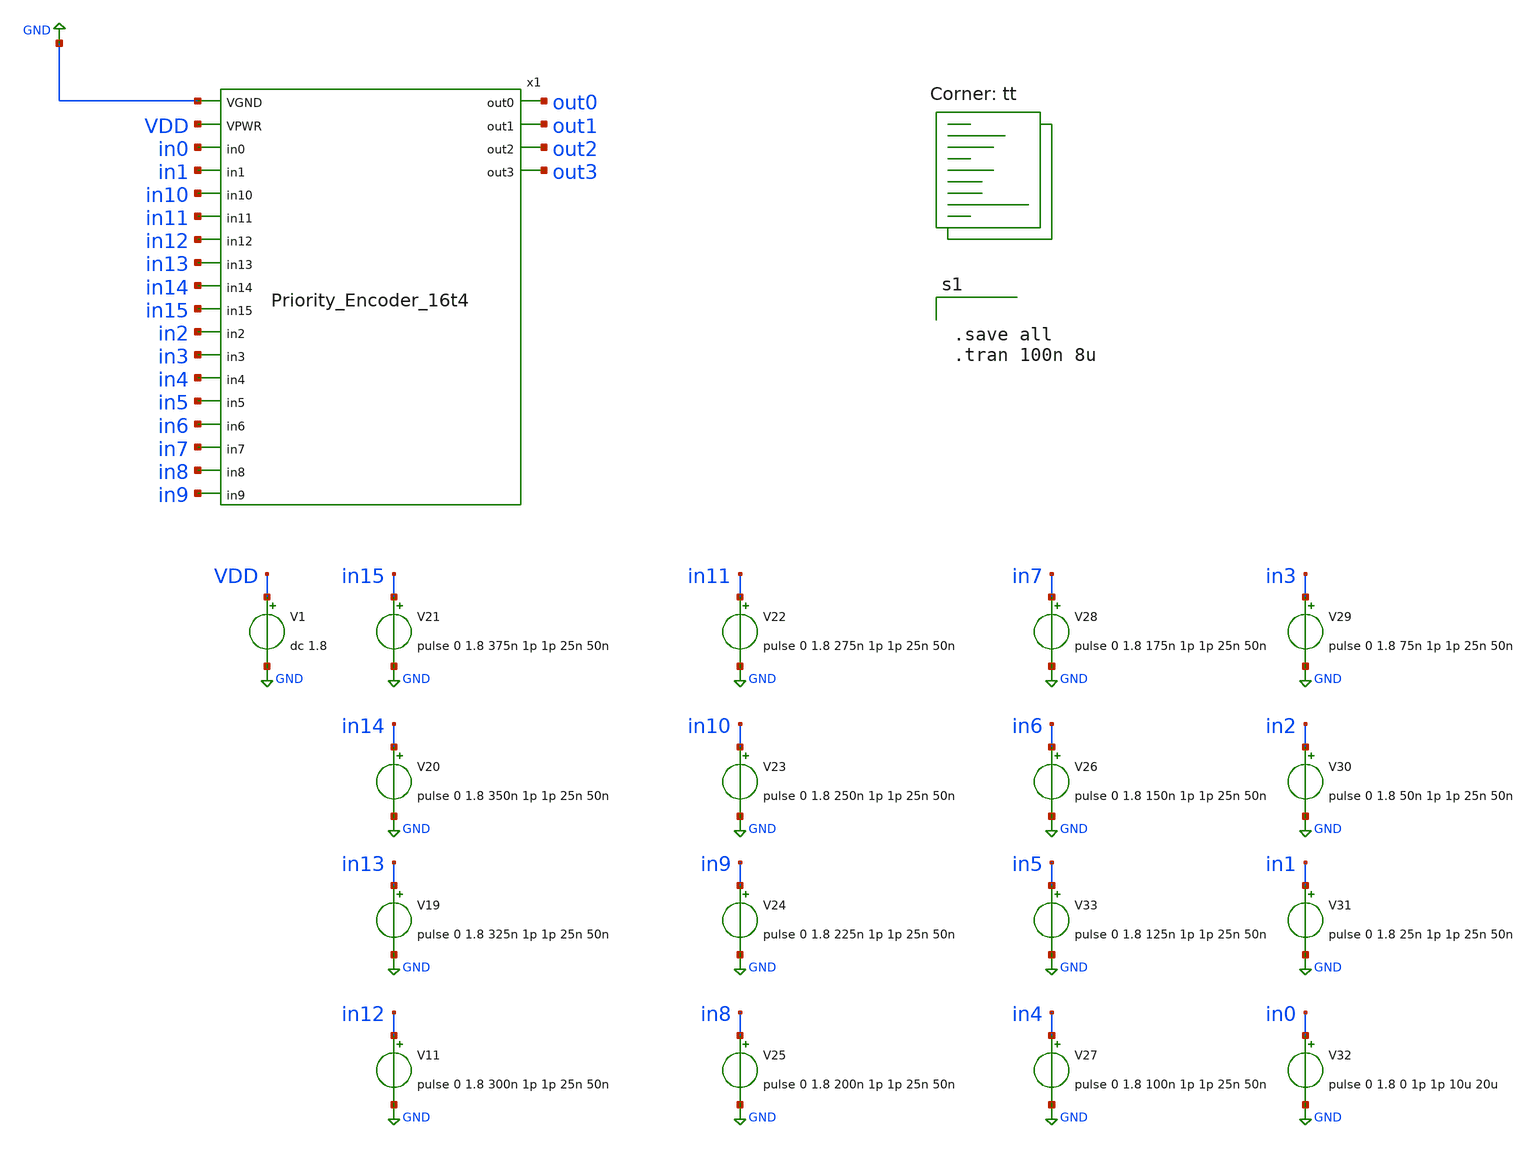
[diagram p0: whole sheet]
** sch_path: xschem/DataConverters/P_Encoder_Test.sch
**.subckt P_Encoder_Test
V1 VDD GND dc 1.8
x1 GND VDD in0 in1 in10 in11 in12 in13 in14 in15 in2 in3 in4 in5 in6 in7 in8 in9 out0 out1 out2 out3
+ Priority_Encoder_16t4
V11 in12 GND pulse 0 1.8 300n 1p 1p 25n 50n
V19 in13 GND pulse 0 1.8 325n 1p 1p 25n 50n
V20 in14 GND pulse 0 1.8 350n 1p 1p 25n 50n
V21 in15 GND pulse 0 1.8 375n 1p 1p 25n 50n
V22 in11 GND pulse 0 1.8 275n 1p 1p 25n 50n
V23 in10 GND pulse 0 1.8 250n 1p 1p 25n 50n
V24 in9 GND pulse 0 1.8 225n 1p 1p 25n 50n
V25 in8 GND pulse 0 1.8 200n 1p 1p 25n 50n
V26 in6 GND pulse 0 1.8 150n 1p 1p 25n 50n
V27 in4 GND pulse 0 1.8 100n 1p 1p 25n 50n
V28 in7 GND pulse 0 1.8 175n 1p 1p 25n 50n
V29 in3 GND pulse 0 1.8 75n 1p 1p 25n 50n
V30 in2 GND pulse 0 1.8 50n 1p 1p 25n 50n
V31 in1 GND pulse 0 1.8 25n 1p 1p 25n 50n
V32 in0 GND pulse 0 1.8 0 1p 1p 10u 20u
V33 in5 GND pulse 0 1.8 125n 1p 1p 25n 50n
**** begin user architecture code
.lib $::SKYWATER_MODELS/sky130.lib.spice tt


.save all
.tran 100n 8u



** opencircuitdesign pdks install
.include $::SKYWATER_STDCELLS/sky130_fd_sc_hd.spice


**** end user architecture code
**.ends

* expanding   symbol:  DataConverters/Priority_Encoder_16t4.sym # of pins=22
** sym_path: xschem/Priority_Encoder_16t4.sym
** sch_path: xschem/Priority_Encoder_16t4.sch
.subckt Priority_Encoder_16t4 VGND VPWR in0 in1 in10 in11 in12 in13 in14 in15 in2 in3 in4 in5 in6
+ in7 in8 in9 out0 out1 out2 out3
*.ipin VGND
*.ipin VPWR
*.ipin in0
*.ipin in1
*.ipin in10
*.ipin in11
*.ipin in12
*.ipin in13
*.ipin in14
*.ipin in15
*.ipin in2
*.ipin in3
*.ipin in4
*.ipin in5
*.ipin in6
*.ipin in7
*.ipin in8
*.ipin in9
*.opin out0
*.opin out1
*.opin out2
*.opin out3
X_16_ net8 VGND VGND VPWR VPWR _00_ sky130_fd_sc_hd__inv_2
X_17_ net4 net5 VGND VGND VPWR VPWR _01_ sky130_fd_sc_hd__nor2_1
X_18_ net4 net5 net6 net7 VGND VGND VPWR VPWR _02_ sky130_fd_sc_hd__or4_1
X_19_ net2 net3 VGND VGND VPWR VPWR _03_ sky130_fd_sc_hd__nor2_1
X_20_ net15 net14 VGND VGND VPWR VPWR _04_ sky130_fd_sc_hd__nor2_1
X_21_ net15 net14 _02_ _03_ VGND VGND VPWR VPWR net19 sky130_fd_sc_hd__or4b_2
X_22_ net11 net10 VGND VGND VPWR VPWR _05_ sky130_fd_sc_hd__nor2_1
X_23_ net13 net11 net10 net12 VGND VGND VPWR VPWR _06_ sky130_fd_sc_hd__or4_1
X_24_ _03_ _04_ _06_ _02_ VGND VGND VPWR VPWR net18 sky130_fd_sc_hd__a31o_1
X_25_ net9 net8 _05_ VGND VGND VPWR VPWR _07_ sky130_fd_sc_hd__o21a_1
X_26_ net13 net12 _07_ _04_ VGND VGND VPWR VPWR _08_ sky130_fd_sc_hd__o31a_1
X_27_ net2 net3 _08_ _01_ VGND VGND VPWR VPWR _09_ sky130_fd_sc_hd__o31a_1
X_28_ net6 net7 _09_ VGND VGND VPWR VPWR net17 sky130_fd_sc_hd__or3_1
X_29_ _00_ net1 net9 VGND VGND VPWR VPWR _10_ sky130_fd_sc_hd__a21oi_1
X_30_ net10 _10_ net11 VGND VGND VPWR VPWR _11_ sky130_fd_sc_hd__o21ba_1
X_31_ net12 _11_ net13 VGND VGND VPWR VPWR _12_ sky130_fd_sc_hd__o21ba_1
X_32_ net14 _12_ net15 VGND VGND VPWR VPWR _13_ sky130_fd_sc_hd__o21ba_1
X_33_ net2 _13_ net3 VGND VGND VPWR VPWR _14_ sky130_fd_sc_hd__o21ba_1
X_34_ net4 _14_ net5 VGND VGND VPWR VPWR _15_ sky130_fd_sc_hd__o21ba_1
X_35_ net6 _15_ net7 VGND VGND VPWR VPWR net16 sky130_fd_sc_hd__o21bai_2
Xinput1 in1 VGND VGND VPWR VPWR net1 sky130_fd_sc_hd__clkbuf_1
Xinput10 in4 VGND VGND VPWR VPWR net10 sky130_fd_sc_hd__buf_1
Xinput11 in5 VGND VGND VPWR VPWR net11 sky130_fd_sc_hd__buf_1
Xinput12 in6 VGND VGND VPWR VPWR net12 sky130_fd_sc_hd__buf_1
Xinput13 in7 VGND VGND VPWR VPWR net13 sky130_fd_sc_hd__clkbuf_1
Xinput14 in8 VGND VGND VPWR VPWR net14 sky130_fd_sc_hd__buf_1
Xinput15 in9 VGND VGND VPWR VPWR net15 sky130_fd_sc_hd__buf_1
Xinput2 in10 VGND VGND VPWR VPWR net2 sky130_fd_sc_hd__buf_1
Xinput3 in11 VGND VGND VPWR VPWR net3 sky130_fd_sc_hd__buf_1
Xinput4 in12 VGND VGND VPWR VPWR net4 sky130_fd_sc_hd__buf_1
Xinput5 in13 VGND VGND VPWR VPWR net5 sky130_fd_sc_hd__buf_1
Xinput6 in14 VGND VGND VPWR VPWR net6 sky130_fd_sc_hd__buf_1
Xinput7 in15 VGND VGND VPWR VPWR net7 sky130_fd_sc_hd__buf_1
Xinput8 in2 VGND VGND VPWR VPWR net8 sky130_fd_sc_hd__buf_1
Xinput9 in3 VGND VGND VPWR VPWR net9 sky130_fd_sc_hd__buf_1
Xoutput16 net16 VGND VGND VPWR VPWR out0 sky130_fd_sc_hd__buf_12
Xoutput17 net17 VGND VGND VPWR VPWR out1 sky130_fd_sc_hd__buf_12
Xoutput18 net18 VGND VGND VPWR VPWR out2 sky130_fd_sc_hd__buf_12
Xoutput19 net19 VGND VGND VPWR VPWR out3 sky130_fd_sc_hd__buf_12
.ends

.GLOBAL GND
.end
